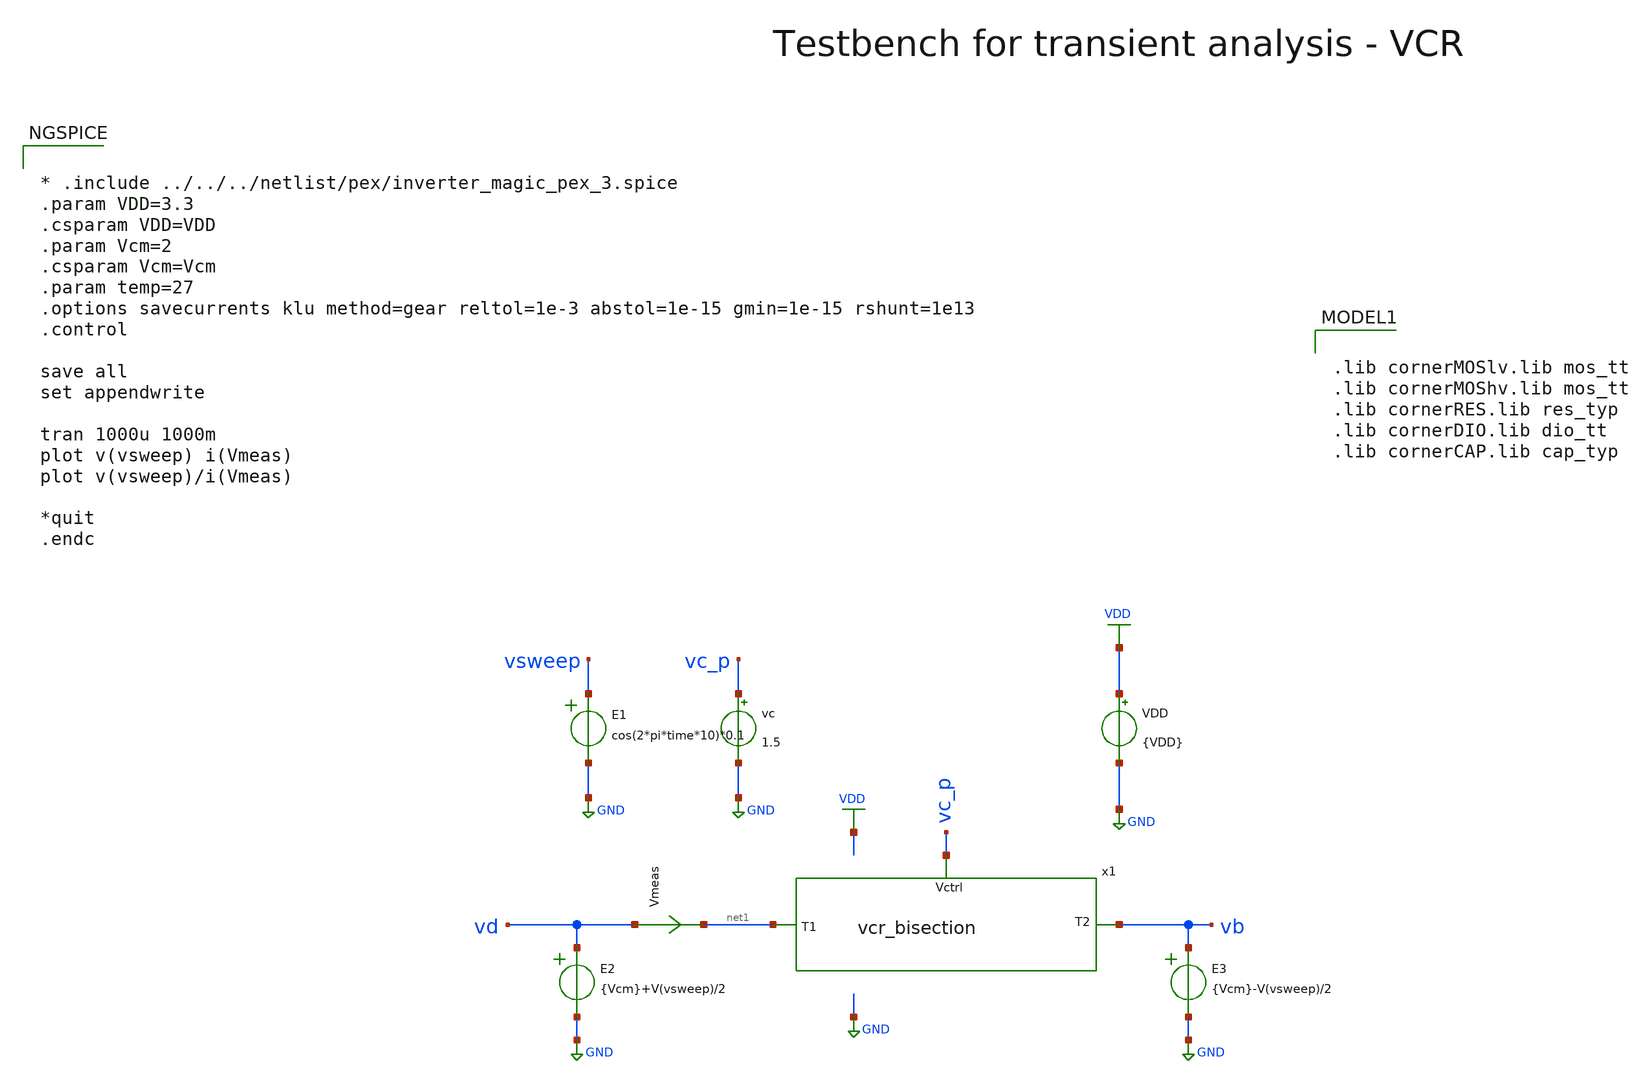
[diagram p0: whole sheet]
** sch_path: macros/heichips26_vcr/macros/vcr_bisection/testbenches/xschem/res_tb_tran.sch
**.subckt res_tb_tran
VDD VDD GND {VDD}
Vmeas vd net1 0
.save i(vmeas)
E2 vd GND VOL=' {Vcm}+V(vsweep)/2 '
E3 vb GND VOL=' {Vcm}-V(vsweep)/2 '
vc vc_p GND 1.5
x1 vc_p net1 vb vcr_bisection
E1 vsweep GND VOL=' cos(2*pi*time*10)*0.1 '
**** begin user architecture code


* .include ../../../netlist/pex/inverter_magic_pex_3.spice
.param VDD=3.3
.csparam VDD=VDD
.param Vcm=2
.csparam Vcm=Vcm
.param temp=27
.options savecurrents klu method=gear reltol=1e-3 abstol=1e-15 gmin=1e-15 rshunt=1e13
.control

save all
set appendwrite

tran 1000u 1000m
plot v(vsweep) i(Vmeas)
plot v(vsweep)/i(Vmeas)

*quit
.endc



.lib cornerMOSlv.lib mos_tt
.lib cornerMOShv.lib mos_tt
.lib cornerRES.lib res_typ
.lib cornerDIO.lib dio_tt
.lib cornerCAP.lib cap_typ

**** end user architecture code
**.ends

* expanding   symbol:  vcr_bisection.sym # of pins=3
** sym_path: macros/heichips26_analog_project/macros/vcr_bisection/schematic/xschem/vcr_bisection.sym
** sch_path: macros/heichips26_analog_project/macros/vcr_bisection/schematic/xschem/vcr_bisection.sch
.subckt vcr_bisection Vctrl T1 T2
*.ipin T1
*.ipin T2
*.ipin Vctrl
R1 vcm T1 10k m=1
R2 T2 vcm 10k m=1
Vmeas T1 net1 0
.save i(vmeas)
XM1 net1 Vctrl T2 vcm sg13_hv_pmos w=50u l=10u ng=10 m=1 mm_ok=1
.ends

.GLOBAL GND
.GLOBAL VDD
.end
